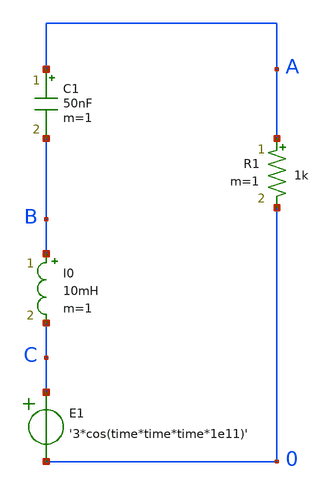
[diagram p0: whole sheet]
** sch_path: xschem_library/examples/rlc.sch
**.subckt rlc
R1 A 0 1k m=1
C1 A B 50nF m=1
l0 B C 10mH m=1
E1 C 0 VOL=' '3*cos(time*time*time*1e11)' '
**** begin user architecture code



.tran 10n 2000u uic
.save all


**** end user architecture code
**.ends
.end
